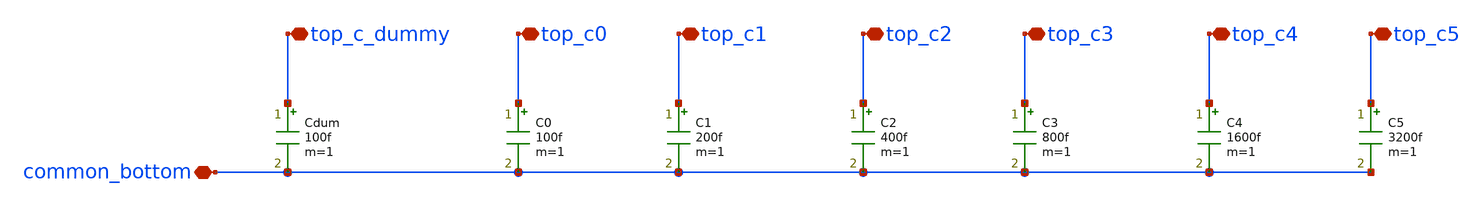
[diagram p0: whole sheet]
** sch_path: xschem/cap_array_MF.sch
**.subckt cap_array_MF common_bottom top_c1 top_c0 top_c_dummy top_c2 top_c4 top_c5 top_c3
*.iopin common_bottom
*.iopin top_c1
*.iopin top_c0
*.iopin top_c_dummy
*.iopin top_c2
*.iopin top_c4
*.iopin top_c5
*.iopin top_c3
Cdum top_c_dummy common_bottom 100f m=1
C0 top_c0 common_bottom 100f m=1
C1 top_c1 common_bottom 200f m=1
C2 top_c2 common_bottom 400f m=1
C3 top_c3 common_bottom 800f m=1
C4 top_c4 common_bottom 1600f m=1
C5 top_c5 common_bottom 3200f m=1
**.ends
.end
